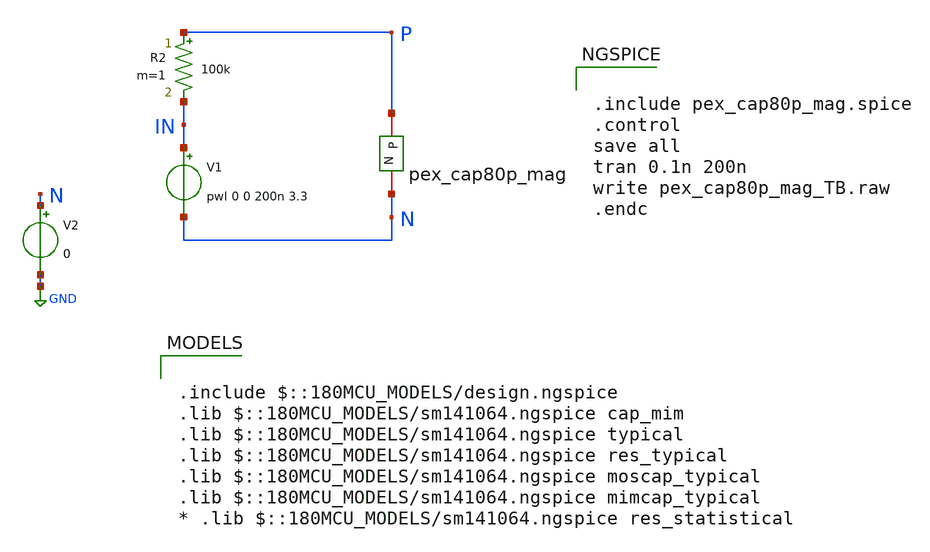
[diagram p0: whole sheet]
** sch_path: Clock_Generator_PAKISTAN_02/Schematics/pex_cap80p_mag_TB.sch
**.subckt pex_cap80p_mag_TB
V1 IN N pwl 0 0 200n 3.3
R2 P IN 100k m=1
V2 N GND 0
x1 N P pex_cap80p_mag
**** begin user architecture code

.include $::180MCU_MODELS/design.ngspice
.lib $::180MCU_MODELS/sm141064.ngspice cap_mim
.lib $::180MCU_MODELS/sm141064.ngspice typical
.lib $::180MCU_MODELS/sm141064.ngspice res_typical
.lib $::180MCU_MODELS/sm141064.ngspice moscap_typical
.lib $::180MCU_MODELS/sm141064.ngspice mimcap_typical
* .lib $::180MCU_MODELS/sm141064.ngspice res_statistical



.include pex_cap80p_mag.spice
.control
save all
tran 0.1n 200n
write pex_cap80p_mag_TB.raw
.endc


**** end user architecture code
**.ends
.GLOBAL GND
.end
